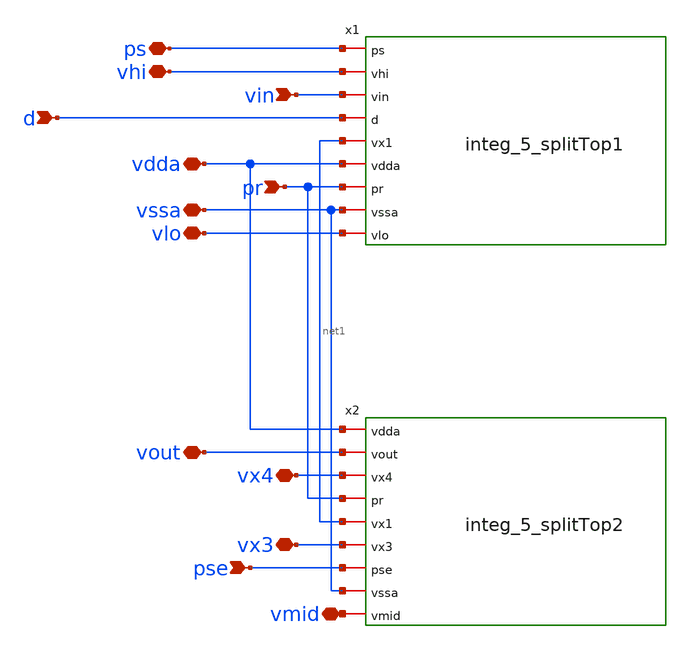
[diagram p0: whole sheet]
** sch_path: 5_Design/4_Layout/Team 5/splitUpSimulationsAndSchematics/integ_5_splitTop3.sch
**.subckt integ_5_splitTop3 pse pr vssa d vlo vin vhi vdda ps vmid vx3 vx4 vout
*.ipin pse
*.ipin pr
*.iopin vssa
*.ipin d
*.iopin vlo
*.ipin vin
*.iopin vhi
*.iopin vdda
*.iopin ps
*.iopin vmid
*.iopin vx3
*.iopin vx4
*.iopin vout
x1 ps vhi vin d net1 vdda pr vssa vlo integ_5_splitTop1
x2 vdda vout vx4 pr net1 vx3 pse vssa vmid integ_5_splitTop2
**.ends
.end
